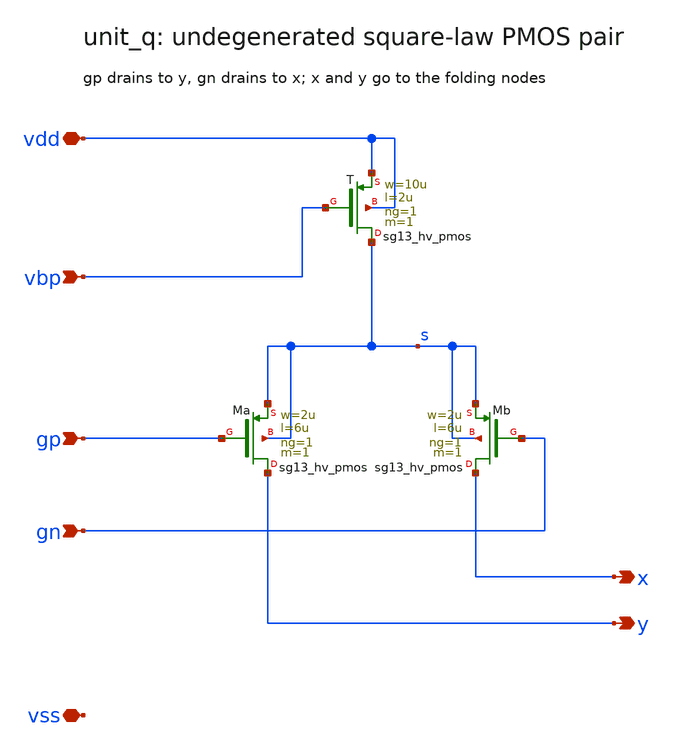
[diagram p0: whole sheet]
** sch_path: sudelbuecher/design_considerations/class_ab_pad_driver/improvements/xschem/unit_q.sch
**.subckt unit_q x y gp gn vdd vss vbp
*.opin x
*.opin y
*.ipin gp
*.ipin gn
*.iopin vdd
*.iopin vss
*.ipin vbp
XT s vbp vdd vdd sg13_hv_pmos w=10u l=2u ng=1 m=1 mm_ok=1
XMa y gp s s sg13_hv_pmos w=2u l=6u ng=1 m=1 mm_ok=1
XMb x gn s s sg13_hv_pmos w=2u l=6u ng=1 m=1 mm_ok=1
**.ends
.end
